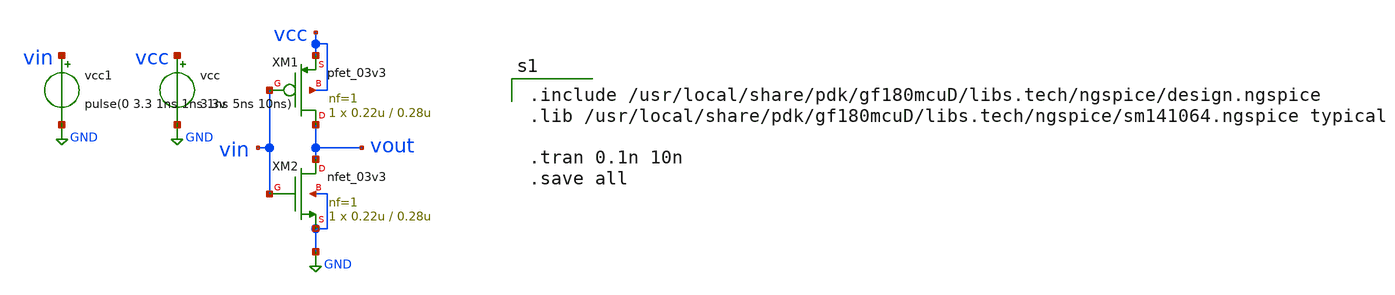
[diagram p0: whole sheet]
** sch_path: schem/untitled.sch
**.subckt untitled
vcc vcc GND 3.3v
vcc1 vin GND pulse(0 3.3 1ns 1ns 1ns 5ns 10ns)
XM1 vout vin vcc vcc pfet_03v3 L=0.28u W=0.22u nf=1 ad='int((nf+1)/2) * W/nf * 0.18u' as='int((nf+2)/2) * W/nf * 0.18u'
+ pd='2*int((nf+1)/2) * (W/nf + 0.18u)' ps='2*int((nf+2)/2) * (W/nf + 0.18u)' nrd='0.18u / W' nrs='0.18u / W'
+ sa=0 sb=0 sd=0 m=1
XM2 vout vin GND GND nfet_03v3 L=0.28u W=0.22u nf=1 ad='int((nf+1)/2) * W/nf * 0.18u' as='int((nf+2)/2) * W/nf * 0.18u'
+ pd='2*int((nf+1)/2) * (W/nf + 0.18u)' ps='2*int((nf+2)/2) * (W/nf + 0.18u)' nrd='0.18u / W' nrs='0.18u / W'
+ sa=0 sb=0 sd=0 m=1
**** begin user architecture code

.include /usr/local/share/pdk/gf180mcuD/libs.tech/ngspice/design.ngspice
.lib /usr/local/share/pdk/gf180mcuD/libs.tech/ngspice/sm141064.ngspice typical

.tran 0.1n 10n
.save all

**** end user architecture code
**.ends
.GLOBAL GND
.end
